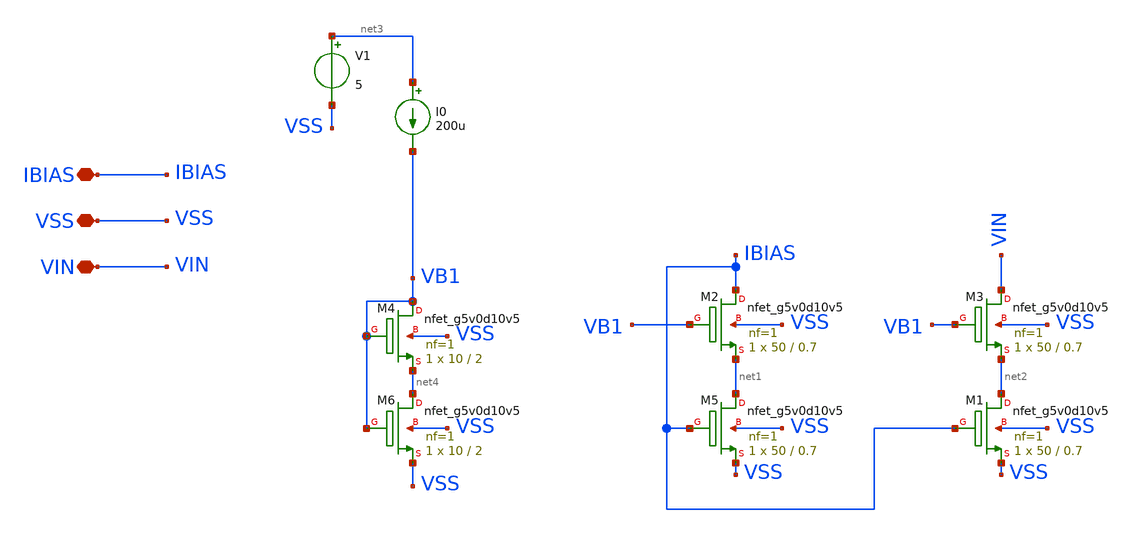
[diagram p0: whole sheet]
** sch_path: amplifiers/current_mirrors/lower_vt_current_mirror/current_mirror.sch
**.subckt current_mirror IBIAS VSS VIN
*.iopin IBIAS
*.iopin VSS
*.iopin VIN
XM5 net1 IBIAS VSS VSS sky130_fd_pr__nfet_g5v0d10v5 L=0.7 W=50 nf=1 ad='int((1 + 1)/2) * 50 / 1 * 0.29'
+ as='int((1 + 2)/2) * 50 / 1 * 0.29' pd='2*int((1 + 1)/2) * (50 / 1 + 0.29)' ps='2*int((1 + 2)/2) * (50 / 1 + 0.29)'
+ nrd='0.29 / 50 ' nrs='0.29 / 50 ' sa=0 sb=0 sd=0 mult=1 m=1
XM1 net2 IBIAS VSS VSS sky130_fd_pr__nfet_g5v0d10v5 L=0.7 W=50 nf=1 ad='int((1 + 1)/2) * 50 / 1 * 0.29'
+ as='int((1 + 2)/2) * 50 / 1 * 0.29' pd='2*int((1 + 1)/2) * (50 / 1 + 0.29)' ps='2*int((1 + 2)/2) * (50 / 1 + 0.29)'
+ nrd='0.29 / 50 ' nrs='0.29 / 50 ' sa=0 sb=0 sd=0 mult=1 m=1
XM2 IBIAS VB1 net1 VSS sky130_fd_pr__nfet_g5v0d10v5 L=0.7 W=50 nf=1 ad='int((1 + 1)/2) * 50 / 1 * 0.29'
+ as='int((1 + 2)/2) * 50 / 1 * 0.29' pd='2*int((1 + 1)/2) * (50 / 1 + 0.29)' ps='2*int((1 + 2)/2) * (50 / 1 + 0.29)'
+ nrd='0.29 / 50 ' nrs='0.29 / 50 ' sa=0 sb=0 sd=0 mult=1 m=1
XM3 VIN VB1 net2 VSS sky130_fd_pr__nfet_g5v0d10v5 L=0.7 W=50 nf=1 ad='int((1 + 1)/2) * 50 / 1 * 0.29'
+ as='int((1 + 2)/2) * 50 / 1 * 0.29' pd='2*int((1 + 1)/2) * (50 / 1 + 0.29)' ps='2*int((1 + 2)/2) * (50 / 1 + 0.29)'
+ nrd='0.29 / 50 ' nrs='0.29 / 50 ' sa=0 sb=0 sd=0 mult=1 m=1
I0 net3 VB1 200u
V1 net3 VSS 5
XM4 VB1 VB1 net4 VSS sky130_fd_pr__nfet_g5v0d10v5 L=2 W=10 nf=1 ad='int((1 + 1)/2) * 10 / 1 * 0.29' as='int((1 + 2)/2) * 10 / 1 * 0.29'
+ pd='2*int((1 + 1)/2) * (10 / 1 + 0.29)' ps='2*int((1 + 2)/2) * (10 / 1 + 0.29)' nrd='0.29 / 10 ' nrs='0.29 / 10 '
+ sa=0 sb=0 sd=0 mult=1 m=1
XM6 net4 VB1 VSS VSS sky130_fd_pr__nfet_g5v0d10v5 L=2 W=10 nf=1 ad='int((1 + 1)/2) * 10 / 1 * 0.29' as='int((1 + 2)/2) * 10 / 1 * 0.29'
+ pd='2*int((1 + 1)/2) * (10 / 1 + 0.29)' ps='2*int((1 + 2)/2) * (10 / 1 + 0.29)' nrd='0.29 / 10 ' nrs='0.29 / 10 '
+ sa=0 sb=0 sd=0 mult=1 m=1
**.ends
.end
